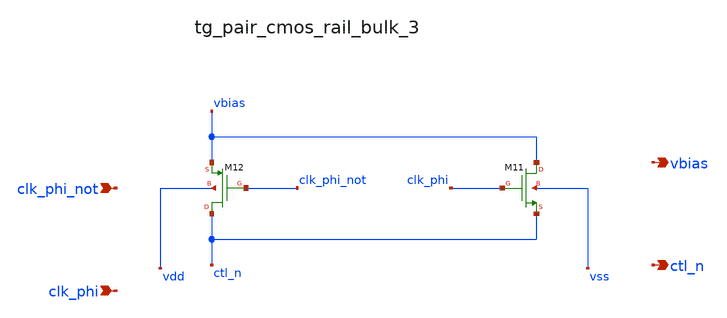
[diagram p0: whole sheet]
** sch_path: analog-db/raw/cmfb_004_output_switched_cap/hier/blocks/tg_pair_cmos_rail_bulk_3.sch
**.subckt tg_pair_cmos_rail_bulk_3 clk_phi_not clk_phi vbias ctl_n
*.ipin clk_phi_not
*.ipin clk_phi
*.opin vbias
*.opin ctl_n
XM11 vbias clk_phi ctl_n vss sg13_lv_nmos w=x_dut_xm11_w l=x_dut_xm11_l ng=1 m=x_dut_xm11_m
XM12 ctl_n clk_phi_not vbias vdd sg13_lv_pmos w=x_dut_xm12_w l=x_dut_xm12_l ng=1 m=x_dut_xm12_m
**.ends
.end
